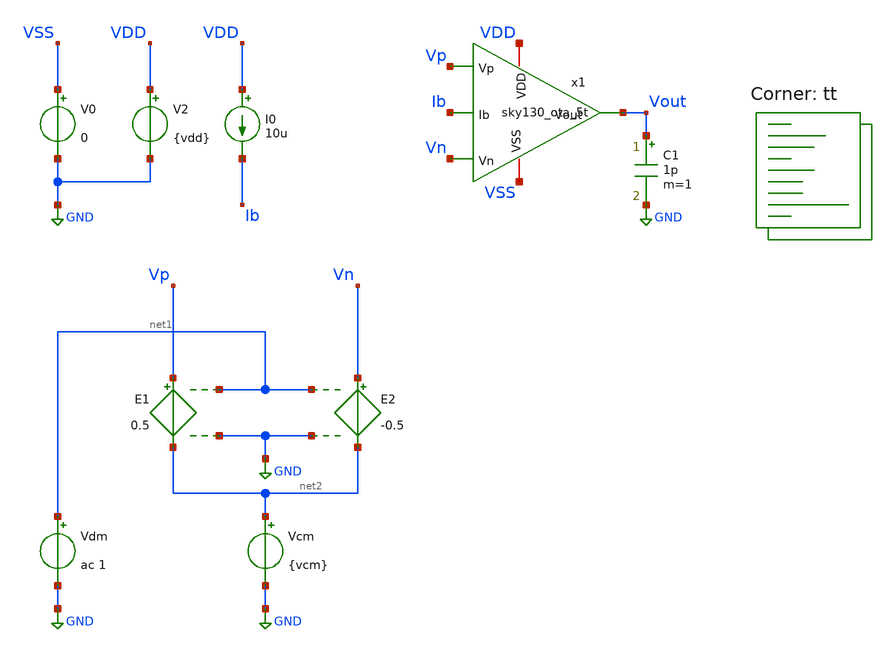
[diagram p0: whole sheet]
** sch_path: xschem/sky130_ota_5t_tb.sch
**.subckt sky130_ota_5t_tb
I0 VDD Ib 10u
C1 Vout GND 1p m=1
V0 VSS GND 0
V2 VDD GND {vdd}
E1 Vp net2 net1 GND 0.5
E2 Vn net2 net1 GND -0.5
Vdm net1 GND ac 1
Vcm net2 GND {vcm}
x1 Vp Vn Vout VDD VSS Ib sky130_ota_5t
**** begin user architecture code


.param vdd=1.8
.param vcm=0.9

.control

    save all

    save @m.x1.xm1.msky130_fd_pr__pfet_01v8[id] @m.x1.xm1.msky130_fd_pr__pfet_01v8[gm]
+ @m.x1.xm1.msky130_fd_pr__pfet_01v8[gds]
    save @m.x1.xm2.msky130_fd_pr__pfet_01v8[id] @m.x1.xm2.msky130_fd_pr__pfet_01v8[gm]
+ @m.x1.xm2.msky130_fd_pr__pfet_01v8[gds]

    save @m.x1.xm3.msky130_fd_pr__nfet_01v8[id] @m.x1.xm3.msky130_fd_pr__nfet_01v8[gm]
+ @m.x1.xm3.msky130_fd_pr__nfet_01v8[gds]
    save @m.x1.xm4.msky130_fd_pr__nfet_01v8[id] @m.x1.xm4.msky130_fd_pr__nfet_01v8[gm]
+ @m.x1.xm4.msky130_fd_pr__nfet_01v8[gds]
    save @m.x1.xm5.msky130_fd_pr__nfet_01v8[id] @m.x1.xm5.msky130_fd_pr__nfet_01v8[gm]
+ @m.x1.xm5.msky130_fd_pr__nfet_01v8[gds]
    save @m.x1.xm6.msky130_fd_pr__nfet_01v8[id] @m.x1.xm6.msky130_fd_pr__nfet_01v8[gm]
+ @m.x1.xm6.msky130_fd_pr__nfet_01v8[gds]

    * operating point
    op

    write sky130_ota_5t_tb.raw
    set appendwrite

    * run ac simulation
    ac dec 20 1k 100e6

    * measure parameters
    let vout_mag = abs(v(Vout))
    let vout_phase_margin = phase(v(Vout)) * 180/pi + 180
    let vout_mag_db = db(vout_mag)
    meas ac A0 find vout_mag at=1k
    meas ac A0dB find vout_mag_db at=1k
    meas ac UGF when vout_mag=1 fall=1
    meas ac PM find vout_phase_margin when vout_mag=1

    write sky130_ota_5t_tb.raw
.endc


.lib $::SKYWATER_MODELS/sky130.lib.spice tt
**** end user architecture code
**.ends

* expanding   symbol:  /foss/designs/sky130_ota_5t/xschem/sky130_ota_5t.sym # of pins=6
** sym_path: xschem/sky130_ota_5t.sym
** sch_path: xschem/sky130_ota_5t.sch
.subckt sky130_ota_5t Vp Vn Vout VDD VSS Ib
*.ipin Vp
*.ipin Vn
*.opin Vout
*.iopin VDD
*.iopin VSS
*.ipin Ib
XM4 net1 Vp node VSS sky130_fd_pr__nfet_01v8 L=0.5 W=20 nf=4 ad='int((nf+1)/2) * W/nf * 0.29' as='int((nf+2)/2) * W/nf * 0.29'
+ pd='2*int((nf+1)/2) * (W/nf + 0.29)' ps='2*int((nf+2)/2) * (W/nf + 0.29)' nrd='0.29 / W' nrs='0.29 / W'
+ sa=0 sb=0 sd=0 mult=1 m=1
XM1 Vout net1 VDD VDD sky130_fd_pr__pfet_01v8 L=1 W=2 nf=2 ad='int((nf+1)/2) * W/nf * 0.29' as='int((nf+2)/2) * W/nf * 0.29'
+ pd='2*int((nf+1)/2) * (W/nf + 0.29)' ps='2*int((nf+2)/2) * (W/nf + 0.29)' nrd='0.29 / W' nrs='0.29 / W'
+ sa=0 sb=0 sd=0 mult=1 m=1
XM2 net1 net1 VDD VDD sky130_fd_pr__pfet_01v8 L=1 W=2 nf=2 ad='int((nf+1)/2) * W/nf * 0.29' as='int((nf+2)/2) * W/nf * 0.29'
+ pd='2*int((nf+1)/2) * (W/nf + 0.29)' ps='2*int((nf+2)/2) * (W/nf + 0.29)' nrd='0.29 / W' nrs='0.29 / W'
+ sa=0 sb=0 sd=0 mult=1 m=1
XM3 Vout Vn node VSS sky130_fd_pr__nfet_01v8 L=0.5 W=20 nf=4 ad='int((nf+1)/2) * W/nf * 0.29' as='int((nf+2)/2) * W/nf * 0.29'
+ pd='2*int((nf+1)/2) * (W/nf + 0.29)' ps='2*int((nf+2)/2) * (W/nf + 0.29)' nrd='0.29 / W' nrs='0.29 / W'
+ sa=0 sb=0 sd=0 mult=1 m=1
XM5 node Ib VSS VSS sky130_fd_pr__nfet_01v8 L=1 W=2 nf=2 ad='int((nf+1)/2) * W/nf * 0.29' as='int((nf+2)/2) * W/nf * 0.29'
+ pd='2*int((nf+1)/2) * (W/nf + 0.29)' ps='2*int((nf+2)/2) * (W/nf + 0.29)' nrd='0.29 / W' nrs='0.29 / W'
+ sa=0 sb=0 sd=0 mult=1 m=1
XM6 Ib Ib VSS VSS sky130_fd_pr__nfet_01v8 L=1 W=2 nf=2 ad='int((nf+1)/2) * W/nf * 0.29' as='int((nf+2)/2) * W/nf * 0.29'
+ pd='2*int((nf+1)/2) * (W/nf + 0.29)' ps='2*int((nf+2)/2) * (W/nf + 0.29)' nrd='0.29 / W' nrs='0.29 / W'
+ sa=0 sb=0 sd=0 mult=1 m=1
XM7 Vout VDD VDD VDD sky130_fd_pr__pfet_01v8 L=1 W=2 nf=2 ad='int((nf+1)/2) * W/nf * 0.29' as='int((nf+2)/2) * W/nf * 0.29'
+ pd='2*int((nf+1)/2) * (W/nf + 0.29)' ps='2*int((nf+2)/2) * (W/nf + 0.29)' nrd='0.29 / W' nrs='0.29 / W'
+ sa=0 sb=0 sd=0 mult=1 m=1
XM8 node VSS VSS VSS sky130_fd_pr__nfet_01v8 L=0.5 W=20 nf=4 ad='int((nf+1)/2) * W/nf * 0.29' as='int((nf+2)/2) * W/nf * 0.29'
+ pd='2*int((nf+1)/2) * (W/nf + 0.29)' ps='2*int((nf+2)/2) * (W/nf + 0.29)' nrd='0.29 / W' nrs='0.29 / W'
+ sa=0 sb=0 sd=0 mult=1 m=1
XM9 node VSS VSS VSS sky130_fd_pr__nfet_01v8 L=1 W=2 nf=2 ad='int((nf+1)/2) * W/nf * 0.29' as='int((nf+2)/2) * W/nf * 0.29'
+ pd='2*int((nf+1)/2) * (W/nf + 0.29)' ps='2*int((nf+2)/2) * (W/nf + 0.29)' nrd='0.29 / W' nrs='0.29 / W'
+ sa=0 sb=0 sd=0 mult=1 m=1
.ends

.GLOBAL GND
.end
